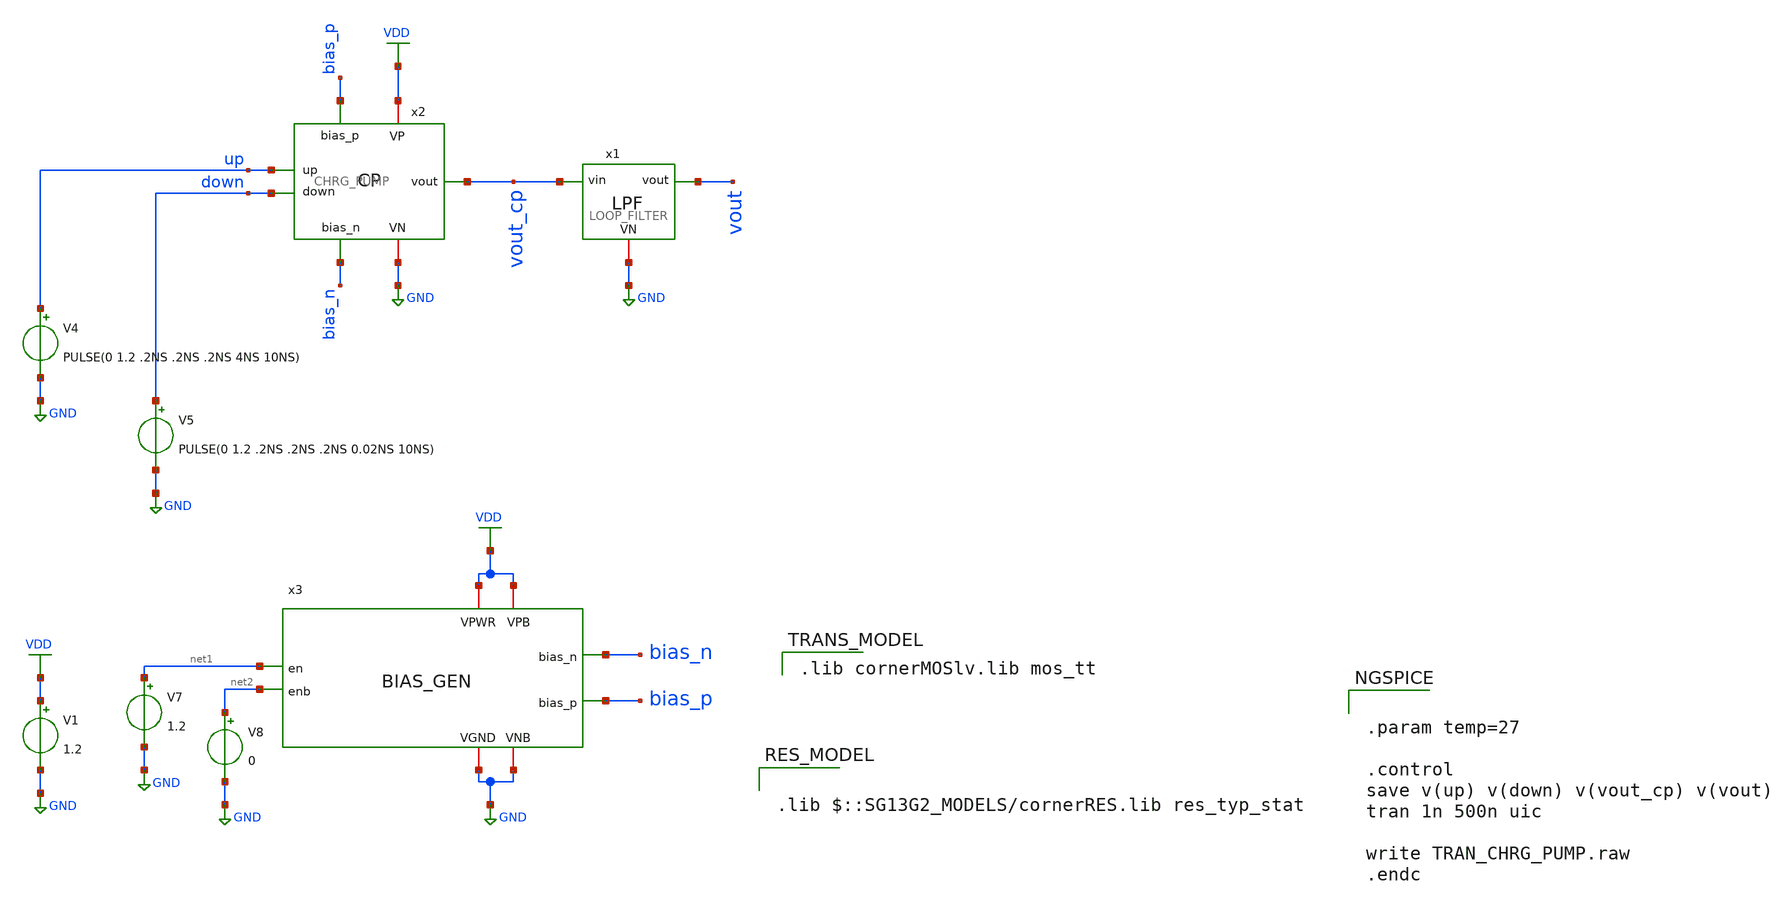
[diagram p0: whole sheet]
** sch_path: 30_MHz_Fractional_N_PLL/design_data/xschem/CHRG_PUMP_TB.sch
**.subckt CHRG_PUMP_TB
V1 VDD GND 1.2
V4 up GND PULSE(0 1.2 .2NS .2NS .2NS 4NS 10NS)
V5 down GND PULSE(0 1.2 .2NS .2NS .2NS 0.02NS 10NS)
x2 VDD bias_p up vout_cp down bias_n GND CHRG_PUMP
x1 vout_cp vout GND LOOP_FILTER
x3 VDD VDD GND GND net1 bias_n bias_p net2 BIAS_GEN
V7 net1 GND 1.2
V8 net2 GND 0
**** begin user architecture code


.param temp=27

.control
save v(up) v(down) v(vout_cp) v(vout)
tran 1n 500n uic

write TRAN_CHRG_PUMP.raw
.endc


 .lib cornerMOSlv.lib mos_tt


.lib $::SG13G2_MODELS/cornerRES.lib res_typ_stat

**** end user architecture code
**.ends

* expanding   symbol:  CHRG_PUMP.sym # of pins=7
** sym_path: 30_MHz_Fractional_N_PLL/design_data/xschem/CHRG_PUMP.sym
** sch_path: 30_MHz_Fractional_N_PLL/design_data/xschem/CHRG_PUMP.sch
.subckt CHRG_PUMP VP bias_p up vout down bias_n VN
*.ipin bias_p
*.ipin up
*.ipin down
*.ipin bias_n
*.iopin VN
*.iopin VP
*.opin vout
XM1 net1 bias_n VN VN sg13_lv_nmos w=1.2u l=0.13u ng=1 m=1 mm_ok=1
XM2 vout down net1 VN sg13_lv_nmos w=1.2u l=0.13u ng=1 m=1 mm_ok=1
XM3 vout net3 net2 VP sg13_lv_pmos w=0.15u l=0.13u ng=1 m=1 mm_ok=1
XM4 net2 bias_p VP VP sg13_lv_pmos w=0.15u l=0.13u ng=1 m=1 mm_ok=1
x1 VP up net3 VN INV
.ends


* expanding   symbol:  LOOP_FILTER.sym # of pins=3
** sym_path: 30_MHz_Fractional_N_PLL/design_data/xschem/LOOP_FILTER.sym
** sch_path: 30_MHz_Fractional_N_PLL/design_data/xschem/LOOP_FILTER.sch
.subckt LOOP_FILTER vin vout VN
*.iopin VN
*.ipin vin
*.opin vout
XR1 vout vin sub! rhigh w=0.6e-6 l=0.96e-6 m=1 b=0 mm_ok=1
XM1 VN net1 VN VN sg13_lv_nmos w=0.5u l=0.650u ng=1 m=15 mm_ok=1
XM2 VN vout VN VN sg13_lv_nmos w=0.15u l=0.13u ng=1 m=1 mm_ok=1
XM3 VN net1 VN VN sg13_lv_nmos w=0.5u l=0.650u ng=1 m=15 mm_ok=1
XM4 VN vout VN VN sg13_lv_nmos w=0.15u l=0.13u ng=1 m=1 mm_ok=1
XR2 net1 vin sub! rhigh w=0.5e-6 l=0.96e-6 m=1 b=0 mm_ok=1
XM5 VN vin VN VN sg13_lv_nmos w=1.5u l=0.650u ng=1 m=15 mm_ok=1
XM6 VN vin VN VN sg13_lv_nmos w=1.5u l=0.650u ng=1 m=15 mm_ok=1
.ends


* expanding   symbol:  BIAS_GEN.sym # of pins=8
** sym_path: 30_MHz_Fractional_N_PLL/design_data/xschem/BIAS_GEN.sym
** sch_path: 30_MHz_Fractional_N_PLL/design_data/xschem/BIAS_GEN.sch
.subckt BIAS_GEN VPWR VPB VGND VNB en bias_n bias_p enb
*.ipin en
*.opin bias_n
*.iopin VNB
*.iopin VGND
*.iopin VPB
*.iopin VPWR
*.ipin enb
*.opin bias_p
XM1 bias_p kick kick_sw VNB sg13_lv_nmos w=0.5u l=0.15u ng=1 m=1 mm_ok=1
XM2 kick_sw en VGND VNB sg13_lv_nmos w=0.5u l=0.15u ng=1 m=1 mm_ok=1
XM3 kick bias_n VGND VNB sg13_lv_nmos w=1.0u l=1.0u ng=1 m=1 mm_ok=1
XM4 bias_p bias_n net1 VNB sg13_lv_nmos w=1.0u l=1.0u ng=1 m=1 mm_ok=1
XM5 bias_n enb VGND VNB sg13_lv_nmos w=0.5u l=0.15u ng=1 m=1 mm_ok=1
XM6 bias_n bias_n VGND VNB sg13_lv_nmos w=1.0u l=1.0u ng=1 m=1 mm_ok=1
XM7 kick kick dio_mid VPB sg13_lv_pmos w=0.5u l=0.15u ng=1 m=1 mm_ok=1
XM8 bias_p bias_p VPWR VPB sg13_lv_pmos w=2.0u l=1.0u ng=1 m=1 mm_ok=1
XM9 bias_p en VPWR VPB sg13_lv_pmos w=0.5u l=0.15u ng=1 m=1 mm_ok=1
XM10 bias_n bias_p res_bot VPB sg13_lv_pmos w=4.0u l=1.0u ng=1 m=1 mm_ok=1
XM11 kick en VPWR VPB sg13_lv_pmos w=0.5u l=0.15u ng=1 m=1 mm_ok=1
XM12 dio_mid dio_mid VPWR VPB sg13_lv_pmos w=0.5u l=0.15u ng=1 m=1 mm_ok=1
XR1 VPWR res_bot sub! rhigh w=1.0e-6 l=12.0e-6 m=1 b=0 mm_ok=1
XR2 net1 VGND sub! rhigh w=1.0e-6 l=12.0e-6 m=1 b=0 mm_ok=1
.ends


* expanding   symbol:  INV.sym # of pins=4
** sym_path: 30_MHz_Fractional_N_PLL/design_data/xschem/INV.sym
** sch_path: 30_MHz_Fractional_N_PLL/design_data/xschem/INV.sch
.subckt INV VP IN OUT VN
*.iopin VN
*.iopin VP
*.ipin IN
*.opin OUT
XM1 OUT IN VN VN sg13_lv_nmos w=0.15u l=0.13u ng=1 m=1 mm_ok=1
XM2 OUT IN VP VP sg13_lv_pmos w=0.3u l=0.13u ng=1 m=1 mm_ok=1
.ends

.GLOBAL GND
.GLOBAL VDD
.end
